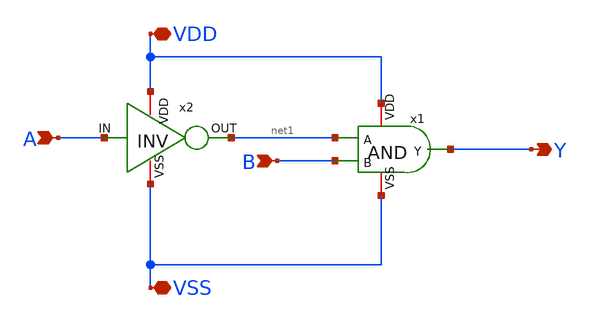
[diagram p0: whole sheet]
** sch_path: untitled.sch
**.subckt untitled A B VDD VSS Y
*.ipin A
*.ipin B
*.iopin VDD
*.iopin VSS
*.opin Y
x1 VDD Y net1 B VSS AND
x2 VDD net1 A VSS INV
**.ends

* expanding   symbol:  AND.sym # of pins=5
** sym_path: AND.sym
** sch_path: AND.sch
.subckt AND VDD Y A B VSS
*.iopin VDD
*.ipin A
*.ipin B
*.iopin VSS
*.opin Y
M1 net1 A net2 VSS nch w=3.5u l=0.35u as=0 ps=0 ad=0 pd=0 m=1
M2 net1 B VDD VDD pch w=3.5u l=0.35u as=0 ps=0 ad=0 pd=0 m=1
M3 net1 A VDD VDD pch w=3.5u l=0.35u as=0 ps=0 ad=0 pd=0 m=1
M4 net2 B VSS VSS nch w=3.5u l=0.35u as=0 ps=0 ad=0 pd=0 m=1
M5 Y net1 VDD VDD pch w=3.5u l=0.35u as=0 ps=0 ad=0 pd=0 m=1
M6 Y net1 VSS VSS nch w=3.5u l=0.35u as=0 ps=0 ad=0 pd=0 m=1
.ends


* expanding   symbol:  INV.sym # of pins=4
** sym_path: INV.sym
** sch_path: INV.sch
.subckt INV VDD OUT IN VSS
*.opin OUT
*.ipin IN
*.iopin VDD
*.iopin VSS
M2 OUT IN VDD VDD pch w=5u l=0.35u as=0 ps=0 ad=0 pd=0 m=1
M1 OUT IN VSS VSS nch w=2.5u l=0.35u as=0 ps=0 ad=0 pd=0 m=1
.ends

.end
